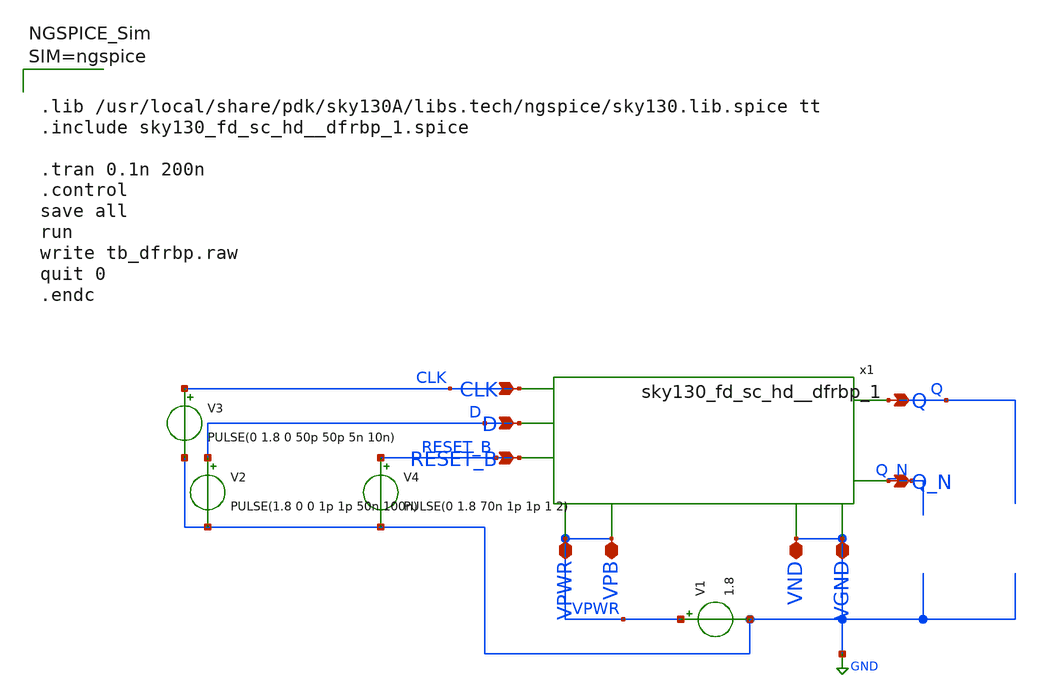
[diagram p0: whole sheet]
** sch_path: sky130_dig_cells/flipflop/tb_dfrbpv4.sch
**.subckt tb_dfrbpv4
x1 CLK D RESET_B GND GND VPWR VPWR Q Q_N sky130_fd_sc_hd__dfrbp_1
V1 VPWR GND 1.8
V2 D GND PULSE(1.8 0 0 1p 1p 50n 100n)
V3 CLK GND PULSE(0 1.8 0 50p 50p 5n 10n)
V4 RESET_B GND PULSE(0 1.8 70n 1p 1p 1 2)
**** begin user architecture code



.lib /usr/local/share/pdk/sky130A/libs.tech/ngspice/sky130.lib.spice tt
.include sky130_fd_sc_hd__dfrbp_1.spice

.tran 0.1n 200n
.control
save all
run
write tb_dfrbp.raw
quit 0
.endc



**** end user architecture code
**.ends
.GLOBAL GND
.end
